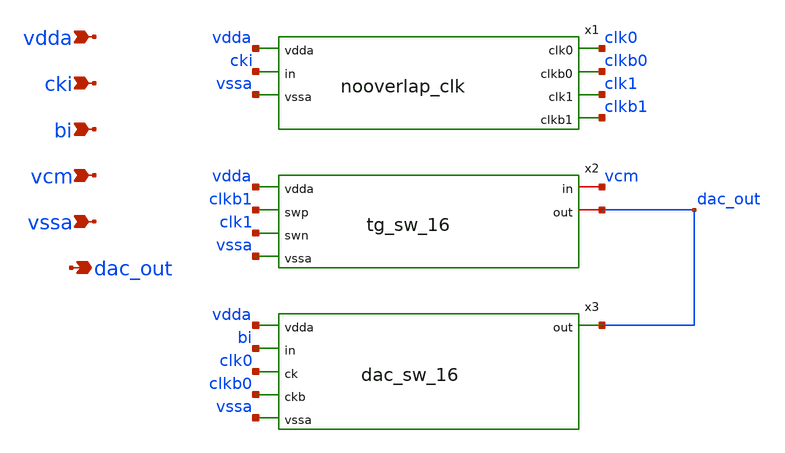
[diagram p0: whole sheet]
** sch_path: top/cdac_sw_16.sch
**.subckt cdac_sw_16 vdda cki bi vcm vssa dac_out
*.ipin vdda
*.ipin cki
*.ipin bi
*.ipin vcm
*.ipin vssa
*.opin dac_out
x1 vdda cki vssa clk0 clkb0 clk1 clkb1 nooverlap_clk
x2 vdda clkb1 clk1 vssa vcm dac_out tg_sw_16
x3 vdda bi clk0 clkb0 vssa dac_out dac_sw_16
**.ends

* expanding   symbol:  nooverlap_clk.sym # of pins=7
** sym_path: top/nooverlap_clk.sym
** sch_path: top/nooverlap_clk.sch
.subckt nooverlap_clk vdda in vssa clk0 clkb0 clk1 clkb1
*.ipin vdda
*.ipin in
*.ipin vssa
*.opin clk0
*.opin clkb0
*.opin clk1
*.opin clkb1
x1 in a vssa vssa vdda vdda net5 sky130_fd_sc_hd__nand2_1
x2 b net1 vssa vssa vdda vdda net2 sky130_fd_sc_hd__nand2_1
x3 in vssa vssa vdda vdda net1 sky130_fd_sc_hd__inv_1
x4 net5 vssa vssa vdda vdda net4 sky130_fd_sc_hd__inv_1
x5 net2 vssa vssa vdda vdda net3 sky130_fd_sc_hd__inv_1
x6 net4 vssa vssa vdda vdda b sky130_fd_sc_hd__inv_1
x7 net3 vssa vssa vdda vdda a sky130_fd_sc_hd__inv_1
x8 b vssa vssa vdda vdda net6 sky130_fd_sc_hd__inv_4
x9 a vssa vssa vdda vdda net7 sky130_fd_sc_hd__inv_4
x10 net6 vssa vssa vdda vdda clkb0 sky130_fd_sc_hd__inv_8
x11 net7 vssa vssa vdda vdda clkb1 sky130_fd_sc_hd__inv_8
x12 clkb0 vssa vssa vdda vdda clk0 sky130_fd_sc_hd__inv_8
x13 clkb1 vssa vssa vdda vdda clk1 sky130_fd_sc_hd__inv_8
.ends


* expanding   symbol:  tg_sw_16.sym # of pins=6
** sym_path: top/tg_sw_16.sym
** sch_path: top/tg_sw_16.sch
.subckt tg_sw_16 vdda swp swn vssa in out
*.ipin vdda
*.ipin swp
*.ipin swn
*.ipin vssa
*.iopin in
*.iopin out
XM1 in swp out vdda sky130_fd_pr__pfet_01v8 L=0.5 W=1.5 nf=1 ad='int((nf+1)/2) * W/nf * 0.29' as='int((nf+2)/2) * W/nf * 0.29'
+ pd='2*int((nf+1)/2) * (W/nf + 0.29)' ps='2*int((nf+2)/2) * (W/nf + 0.29)' nrd='0.29 / W' nrs='0.29 / W'
+ sa=0 sb=0 sd=0 mult=16 m=16
XM2 in swn out vssa sky130_fd_pr__nfet_01v8 L=0.5 W=0.5 nf=1 ad='int((nf+1)/2) * W/nf * 0.29' as='int((nf+2)/2) * W/nf * 0.29'
+ pd='2*int((nf+1)/2) * (W/nf + 0.29)' ps='2*int((nf+2)/2) * (W/nf + 0.29)' nrd='0.29 / W' nrs='0.29 / W'
+ sa=0 sb=0 sd=0 mult=16 m=16
.ends


* expanding   symbol:  dac_sw_16.sym # of pins=6
** sym_path: top/dac_sw_16.sym
** sch_path: top/dac_sw_16.sch
.subckt dac_sw_16 vdda in ck ckb vssa out
*.ipin vdda
*.ipin in
*.ipin ck
*.ipin ckb
*.ipin vssa
*.opin out
XM1 net1 in vdda vdda sky130_fd_pr__pfet_01v8 L=0.5 W=1.5 nf=1 ad='int((nf+1)/2) * W/nf * 0.29' as='int((nf+2)/2) * W/nf * 0.29'
+ pd='2*int((nf+1)/2) * (W/nf + 0.29)' ps='2*int((nf+2)/2) * (W/nf + 0.29)' nrd='0.29 / W' nrs='0.29 / W'
+ sa=0 sb=0 sd=0 mult=16 m=16
XM2 out ckb net1 vdda sky130_fd_pr__pfet_01v8 L=0.5 W=1.5 nf=1 ad='int((nf+1)/2) * W/nf * 0.29' as='int((nf+2)/2) * W/nf * 0.29'
+ pd='2*int((nf+1)/2) * (W/nf + 0.29)' ps='2*int((nf+2)/2) * (W/nf + 0.29)' nrd='0.29 / W' nrs='0.29 / W'
+ sa=0 sb=0 sd=0 mult=16 m=16
XM3 out ck net2 vssa sky130_fd_pr__nfet_01v8 L=0.5 W=0.5 nf=1 ad='int((nf+1)/2) * W/nf * 0.29' as='int((nf+2)/2) * W/nf * 0.29'
+ pd='2*int((nf+1)/2) * (W/nf + 0.29)' ps='2*int((nf+2)/2) * (W/nf + 0.29)' nrd='0.29 / W' nrs='0.29 / W'
+ sa=0 sb=0 sd=0 mult=16 m=16
XM4 net2 in vssa vssa sky130_fd_pr__nfet_01v8 L=0.5 W=0.5 nf=1 ad='int((nf+1)/2) * W/nf * 0.29' as='int((nf+2)/2) * W/nf * 0.29'
+ pd='2*int((nf+1)/2) * (W/nf + 0.29)' ps='2*int((nf+2)/2) * (W/nf + 0.29)' nrd='0.29 / W' nrs='0.29 / W'
+ sa=0 sb=0 sd=0 mult=16 m=16
.ends

.end
